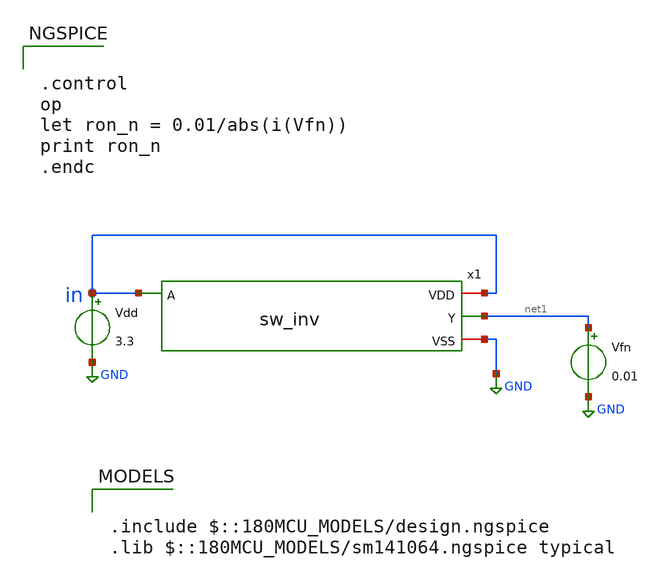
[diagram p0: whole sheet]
** sch_path: xschem/pll_dac/tb_sw_inv.sch
**.subckt tb_sw_inv
x1 in in net1 GND sw_inv
Vdd in GND 3.3
Vfn net1 GND 0.01
**** begin user architecture code

.include $::180MCU_MODELS/design.ngspice
.lib $::180MCU_MODELS/sm141064.ngspice typical



.control
op
let ron_n = 0.01/abs(i(Vfn))
print ron_n
.endc


**** end user architecture code
**.ends

* expanding   symbol:  pll_dac/sw_inv.sym # of pins=4
** sym_path: xschem/pll_dac/sw_inv.sym
** sch_path: xschem/pll_dac/sw_inv.sch
.subckt sw_inv VDD A Y VSS
*.ipin A
*.iopin VDD
*.iopin VSS
*.opin Y
XM1 Y A VSS VSS nfet_03v3 L=0.28u W=2u nf=1 ad='int((nf+1)/2) * W/nf * 0.18u' as='int((nf+2)/2) * W/nf * 0.18u'
+ pd='2*int((nf+1)/2) * (W/nf + 0.18u)' ps='2*int((nf+2)/2) * (W/nf + 0.18u)' nrd='0.18u / W' nrs='0.18u / W'
+ sa=0 sb=0 sd=0 m=1
XM2 Y A VDD VDD pfet_03v3 L=0.28u W=5.6u nf=1 ad='int((nf+1)/2) * W/nf * 0.18u' as='int((nf+2)/2) * W/nf * 0.18u'
+ pd='2*int((nf+1)/2) * (W/nf + 0.18u)' ps='2*int((nf+2)/2) * (W/nf + 0.18u)' nrd='0.18u / W' nrs='0.18u / W'
+ sa=0 sb=0 sd=0 m=1
.ends

.GLOBAL GND
.end
